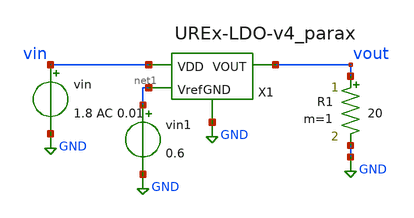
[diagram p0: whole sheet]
** sch_path: xschem/testbenches/postlayout/PSRR-v4-postlayout.sch
**.subckt PSRR-v4-postlayout
vin vin GND 1.8 AC 0.01
X1 vin vout GND net1 UREx-LDO-v4_parax
R1 vout GND 20 m=1
vin1 net1 GND 0.6
**** begin user architecture code



.lib /usr/local/share/pdk/sky130A/libs.tech/ngspice/sky130.lib.spice tt
.ac dec 20 1 1e12
*.tran 1u 5m

.control
run
plot db(vout/vin)
.endc


**** end user architecture code
**.ends

* expanding   symbol:  UREx-LDO-v4_parax.sym # of pins=4
** sym_path: xschem/UREx-LDO-v4.sym
.include [file normalize UREx-LDO-v4_parax.spice]
.GLOBAL GND
.end
